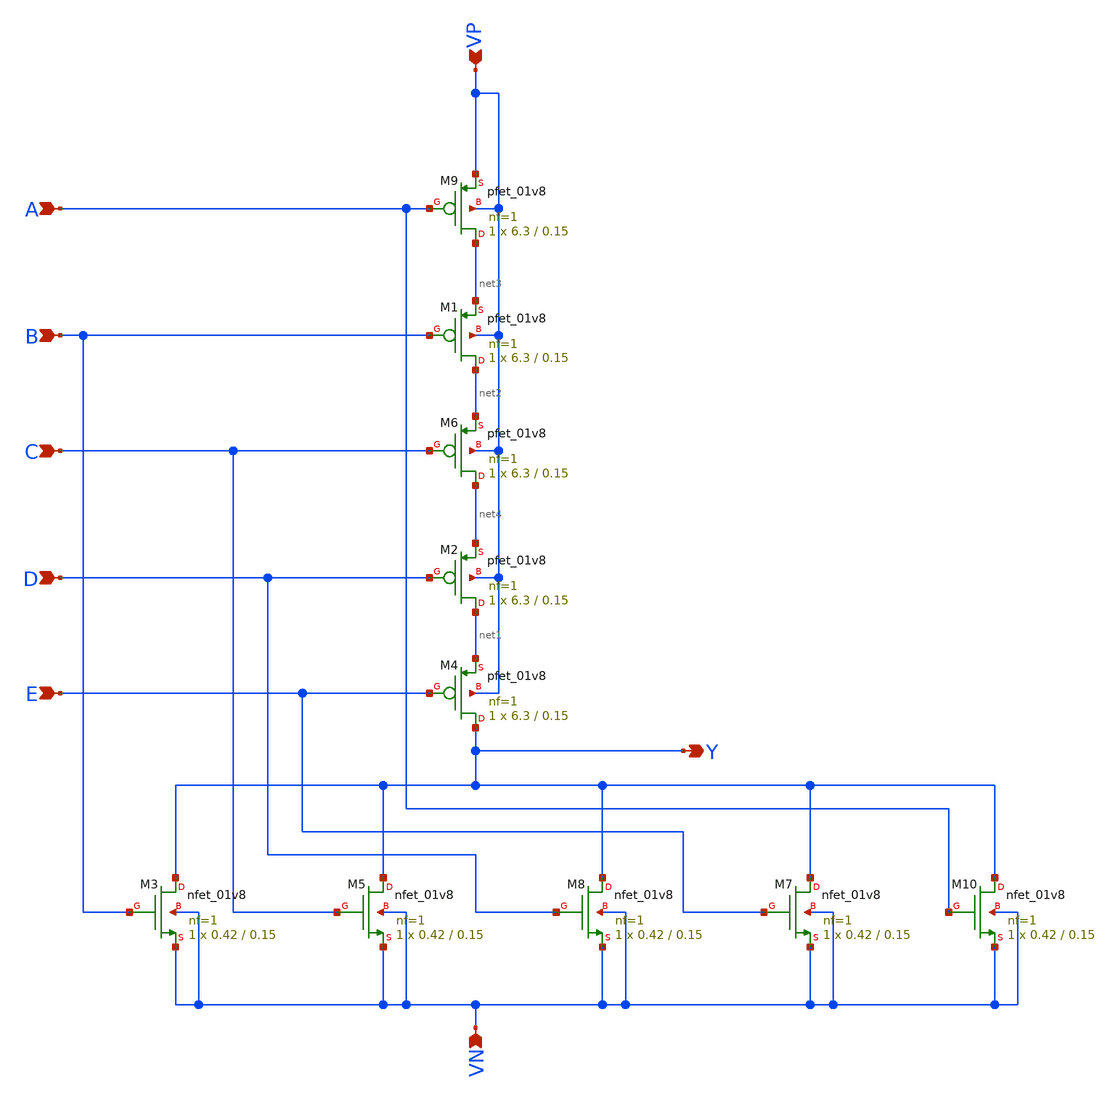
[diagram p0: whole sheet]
** sch_path: component/NOR5/nor5.sch
**.subckt nor5 Y D E B C A VP VN
*.opin Y
*.ipin D
*.ipin E
*.ipin B
*.ipin C
*.ipin A
*.ipin VP
*.ipin VN
XM5 Y C VN VN sky130_fd_pr__nfet_01v8 L=0.15 W=0.42 nf=1 ad='int((nf+1)/2) * W/nf * 0.29' as='int((nf+2)/2) * W/nf * 0.29'
+ pd='2*int((nf+1)/2) * (W/nf + 0.29)' ps='2*int((nf+2)/2) * (W/nf + 0.29)' nrd='0.29 / W' nrs='0.29 / W'
+ sa=0 sb=0 sd=0 mult=1 m=1
XM3 Y B VN VN sky130_fd_pr__nfet_01v8 L=0.15 W=0.42 nf=1 ad='int((nf+1)/2) * W/nf * 0.29' as='int((nf+2)/2) * W/nf * 0.29'
+ pd='2*int((nf+1)/2) * (W/nf + 0.29)' ps='2*int((nf+2)/2) * (W/nf + 0.29)' nrd='0.29 / W' nrs='0.29 / W'
+ sa=0 sb=0 sd=0 mult=1 m=1
XM2 net1 D net4 VP sky130_fd_pr__pfet_01v8 L=0.15 W=6.3 nf=1 ad='int((nf+1)/2) * W/nf * 0.29' as='int((nf+2)/2) * W/nf * 0.29'
+ pd='2*int((nf+1)/2) * (W/nf + 0.29)' ps='2*int((nf+2)/2) * (W/nf + 0.29)' nrd='0.29 / W' nrs='0.29 / W'
+ sa=0 sb=0 sd=0 mult=1 m=1
XM4 Y E net1 VP sky130_fd_pr__pfet_01v8 L=0.15 W=6.3 nf=1 ad='int((nf+1)/2) * W/nf * 0.29' as='int((nf+2)/2) * W/nf * 0.29'
+ pd='2*int((nf+1)/2) * (W/nf + 0.29)' ps='2*int((nf+2)/2) * (W/nf + 0.29)' nrd='0.29 / W' nrs='0.29 / W'
+ sa=0 sb=0 sd=0 mult=1 m=1
XM1 net2 B net3 VP sky130_fd_pr__pfet_01v8 L=0.15 W=6.3 nf=1 ad='int((nf+1)/2) * W/nf * 0.29' as='int((nf+2)/2) * W/nf * 0.29'
+ pd='2*int((nf+1)/2) * (W/nf + 0.29)' ps='2*int((nf+2)/2) * (W/nf + 0.29)' nrd='0.29 / W' nrs='0.29 / W'
+ sa=0 sb=0 sd=0 mult=1 m=1
XM6 net4 C net2 VP sky130_fd_pr__pfet_01v8 L=0.15 W=6.3 nf=1 ad='int((nf+1)/2) * W/nf * 0.29' as='int((nf+2)/2) * W/nf * 0.29'
+ pd='2*int((nf+1)/2) * (W/nf + 0.29)' ps='2*int((nf+2)/2) * (W/nf + 0.29)' nrd='0.29 / W' nrs='0.29 / W'
+ sa=0 sb=0 sd=0 mult=1 m=1
XM7 Y E VN VN sky130_fd_pr__nfet_01v8 L=0.15 W=0.42 nf=1 ad='int((nf+1)/2) * W/nf * 0.29' as='int((nf+2)/2) * W/nf * 0.29'
+ pd='2*int((nf+1)/2) * (W/nf + 0.29)' ps='2*int((nf+2)/2) * (W/nf + 0.29)' nrd='0.29 / W' nrs='0.29 / W'
+ sa=0 sb=0 sd=0 mult=1 m=1
XM8 Y D VN VN sky130_fd_pr__nfet_01v8 L=0.15 W=0.42 nf=1 ad='int((nf+1)/2) * W/nf * 0.29' as='int((nf+2)/2) * W/nf * 0.29'
+ pd='2*int((nf+1)/2) * (W/nf + 0.29)' ps='2*int((nf+2)/2) * (W/nf + 0.29)' nrd='0.29 / W' nrs='0.29 / W'
+ sa=0 sb=0 sd=0 mult=1 m=1
XM9 net3 A VP VP sky130_fd_pr__pfet_01v8 L=0.15 W=6.3 nf=1 ad='int((nf+1)/2) * W/nf * 0.29' as='int((nf+2)/2) * W/nf * 0.29'
+ pd='2*int((nf+1)/2) * (W/nf + 0.29)' ps='2*int((nf+2)/2) * (W/nf + 0.29)' nrd='0.29 / W' nrs='0.29 / W'
+ sa=0 sb=0 sd=0 mult=1 m=1
XM10 Y A VN VN sky130_fd_pr__nfet_01v8 L=0.15 W=0.42 nf=1 ad='int((nf+1)/2) * W/nf * 0.29' as='int((nf+2)/2) * W/nf * 0.29'
+ pd='2*int((nf+1)/2) * (W/nf + 0.29)' ps='2*int((nf+2)/2) * (W/nf + 0.29)' nrd='0.29 / W' nrs='0.29 / W'
+ sa=0 sb=0 sd=0 mult=1 m=1
**.ends
.end
